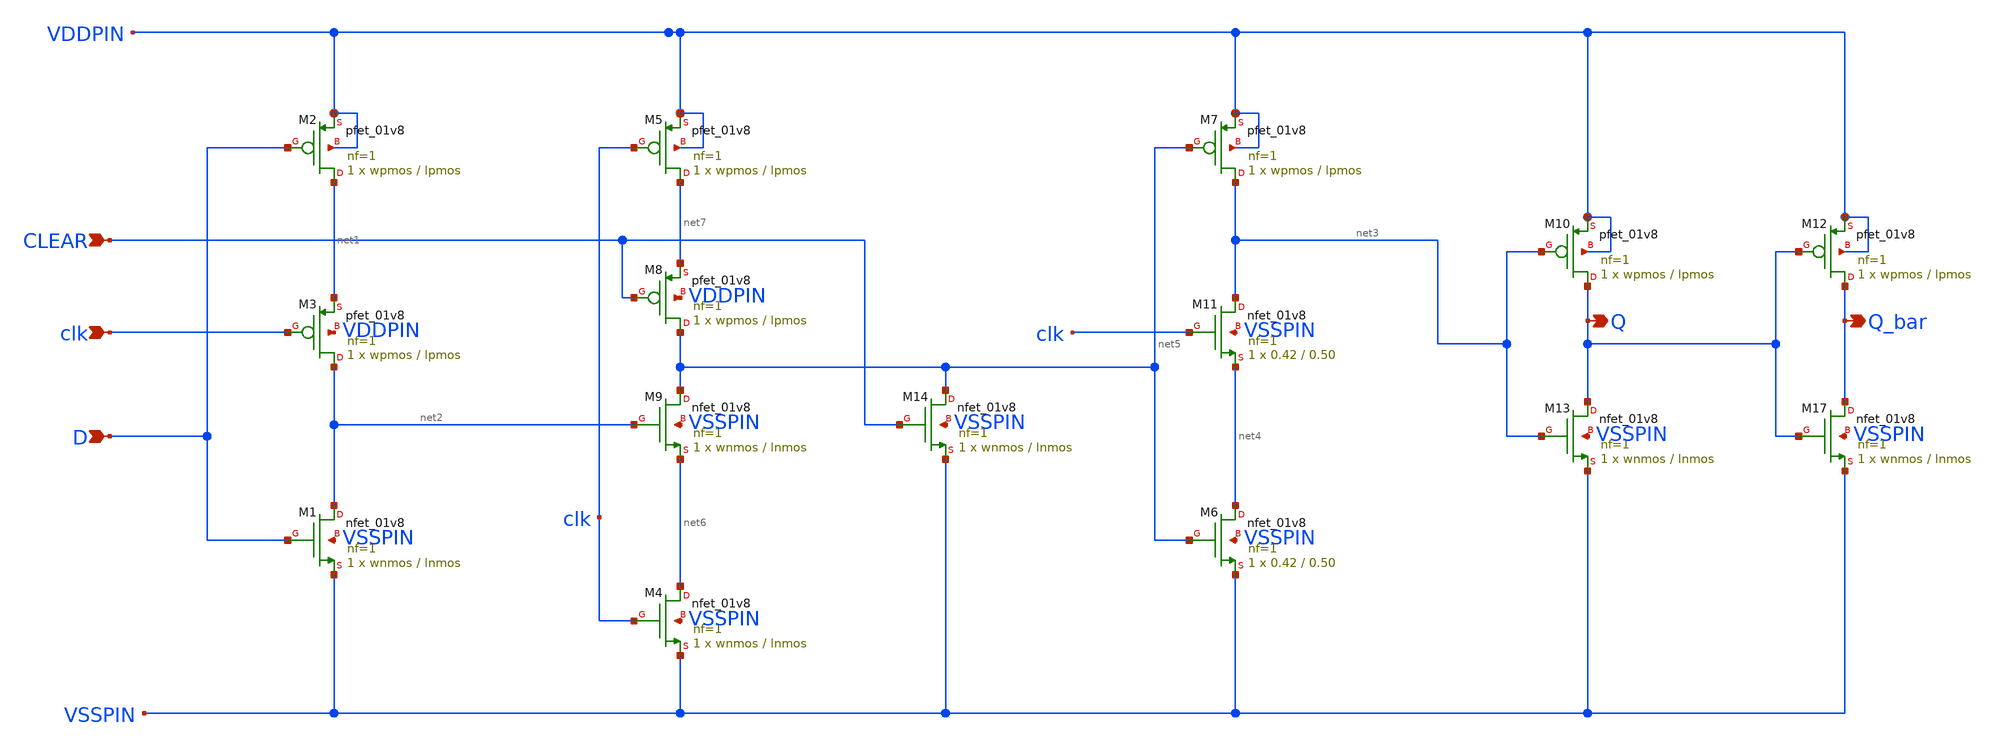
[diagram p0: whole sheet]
** sch_path: TSPC_Dff_with_asynch_clear.sch
**.subckt TSPC_Dff_with_asynch_clear D clk Q Q_bar CLEAR
*.ipin D
*.ipin clk
*.opin Q
*.opin Q_bar
*.ipin CLEAR
XM1 net2 D VSSPIN VSSPIN sky130_fd_pr__nfet_01v8 L=lnmos W=wnmos nf=1 ad='int((nf+1)/2) * W/nf * 0.29'
+ as='int((nf+2)/2) * W/nf * 0.29' pd='2*int((nf+1)/2) * (W/nf + 0.29)' ps='2*int((nf+2)/2) * (W/nf + 0.29)'
+ nrd='0.29 / W' nrs='0.29 / W' sa=0 sb=0 sd=0 mult=1 m=1
XM2 net1 D VDDPIN VDDPIN sky130_fd_pr__pfet_01v8 L=lpmos W=wpmos nf=1 ad='int((nf+1)/2) * W/nf * 0.29'
+ as='int((nf+2)/2) * W/nf * 0.29' pd='2*int((nf+1)/2) * (W/nf + 0.29)' ps='2*int((nf+2)/2) * (W/nf + 0.29)'
+ nrd='0.29 / W' nrs='0.29 / W' sa=0 sb=0 sd=0 mult=1 m=1
XM3 net2 clk net1 VDDPIN sky130_fd_pr__pfet_01v8 L=lpmos W=wpmos nf=1 ad='int((nf+1)/2) * W/nf * 0.29'
+ as='int((nf+2)/2) * W/nf * 0.29' pd='2*int((nf+1)/2) * (W/nf + 0.29)' ps='2*int((nf+2)/2) * (W/nf + 0.29)'
+ nrd='0.29 / W' nrs='0.29 / W' sa=0 sb=0 sd=0 mult=1 m=1
XM4 net6 clk VSSPIN VSSPIN sky130_fd_pr__nfet_01v8 L=lnmos W=wnmos nf=1 ad='int((nf+1)/2) * W/nf * 0.29'
+ as='int((nf+2)/2) * W/nf * 0.29' pd='2*int((nf+1)/2) * (W/nf + 0.29)' ps='2*int((nf+2)/2) * (W/nf + 0.29)'
+ nrd='0.29 / W' nrs='0.29 / W' sa=0 sb=0 sd=0 mult=1 m=1
XM5 net7 clk VDDPIN VDDPIN sky130_fd_pr__pfet_01v8 L=lpmos W=wpmos nf=1 ad='int((nf+1)/2) * W/nf * 0.29'
+ as='int((nf+2)/2) * W/nf * 0.29' pd='2*int((nf+1)/2) * (W/nf + 0.29)' ps='2*int((nf+2)/2) * (W/nf + 0.29)'
+ nrd='0.29 / W' nrs='0.29 / W' sa=0 sb=0 sd=0 mult=1 m=1
XM6 net4 net5 VSSPIN VSSPIN sky130_fd_pr__nfet_01v8 L=0.50 W=0.42 nf=1 ad='int((nf+1)/2) * W/nf * 0.29'
+ as='int((nf+2)/2) * W/nf * 0.29' pd='2*int((nf+1)/2) * (W/nf + 0.29)' ps='2*int((nf+2)/2) * (W/nf + 0.29)'
+ nrd='0.29 / W' nrs='0.29 / W' sa=0 sb=0 sd=0 mult=1 m=1
XM7 net3 net5 VDDPIN VDDPIN sky130_fd_pr__pfet_01v8 L=lpmos W=wpmos nf=1 ad='int((nf+1)/2) * W/nf * 0.29'
+ as='int((nf+2)/2) * W/nf * 0.29' pd='2*int((nf+1)/2) * (W/nf + 0.29)' ps='2*int((nf+2)/2) * (W/nf + 0.29)'
+ nrd='0.29 / W' nrs='0.29 / W' sa=0 sb=0 sd=0 mult=1 m=1
XM9 net5 net2 net6 VSSPIN sky130_fd_pr__nfet_01v8 L=lnmos W=wnmos nf=1 ad='int((nf+1)/2) * W/nf * 0.29'
+ as='int((nf+2)/2) * W/nf * 0.29' pd='2*int((nf+1)/2) * (W/nf + 0.29)' ps='2*int((nf+2)/2) * (W/nf + 0.29)'
+ nrd='0.29 / W' nrs='0.29 / W' sa=0 sb=0 sd=0 mult=1 m=1
XM11 net3 clk net4 VSSPIN sky130_fd_pr__nfet_01v8 L=0.50 W=0.42 nf=1 ad='int((nf+1)/2) * W/nf * 0.29'
+ as='int((nf+2)/2) * W/nf * 0.29' pd='2*int((nf+1)/2) * (W/nf + 0.29)' ps='2*int((nf+2)/2) * (W/nf + 0.29)'
+ nrd='0.29 / W' nrs='0.29 / W' sa=0 sb=0 sd=0 mult=1 m=1
XM10 Q net3 VDDPIN VDDPIN sky130_fd_pr__pfet_01v8 L=lpmos W=wpmos nf=1 ad='int((nf+1)/2) * W/nf * 0.29'
+ as='int((nf+2)/2) * W/nf * 0.29' pd='2*int((nf+1)/2) * (W/nf + 0.29)' ps='2*int((nf+2)/2) * (W/nf + 0.29)'
+ nrd='0.29 / W' nrs='0.29 / W' sa=0 sb=0 sd=0 mult=1 m=1
XM13 Q net3 VSSPIN VSSPIN sky130_fd_pr__nfet_01v8 L=lnmos W=wnmos nf=1 ad='int((nf+1)/2) * W/nf * 0.29'
+ as='int((nf+2)/2) * W/nf * 0.29' pd='2*int((nf+1)/2) * (W/nf + 0.29)' ps='2*int((nf+2)/2) * (W/nf + 0.29)'
+ nrd='0.29 / W' nrs='0.29 / W' sa=0 sb=0 sd=0 mult=1 m=1
XM12 Q_bar Q VDDPIN VDDPIN sky130_fd_pr__pfet_01v8 L=lpmos W=wpmos nf=1 ad='int((nf+1)/2) * W/nf * 0.29'
+ as='int((nf+2)/2) * W/nf * 0.29' pd='2*int((nf+1)/2) * (W/nf + 0.29)' ps='2*int((nf+2)/2) * (W/nf + 0.29)'
+ nrd='0.29 / W' nrs='0.29 / W' sa=0 sb=0 sd=0 mult=1 m=1
XM17 Q_bar Q VSSPIN VSSPIN sky130_fd_pr__nfet_01v8 L=lnmos W=wnmos nf=1 ad='int((nf+1)/2) * W/nf * 0.29'
+ as='int((nf+2)/2) * W/nf * 0.29' pd='2*int((nf+1)/2) * (W/nf + 0.29)' ps='2*int((nf+2)/2) * (W/nf + 0.29)'
+ nrd='0.29 / W' nrs='0.29 / W' sa=0 sb=0 sd=0 mult=1 m=1
XM8 net5 CLEAR net7 VDDPIN sky130_fd_pr__pfet_01v8 L=lpmos W=wpmos nf=1 ad='int((nf+1)/2) * W/nf * 0.29'
+ as='int((nf+2)/2) * W/nf * 0.29' pd='2*int((nf+1)/2) * (W/nf + 0.29)' ps='2*int((nf+2)/2) * (W/nf + 0.29)'
+ nrd='0.29 / W' nrs='0.29 / W' sa=0 sb=0 sd=0 mult=1 m=1
XM14 net5 CLEAR VSSPIN VSSPIN sky130_fd_pr__nfet_01v8 L=lnmos W=wnmos nf=1 ad='int((nf+1)/2) * W/nf * 0.29'
+ as='int((nf+2)/2) * W/nf * 0.29' pd='2*int((nf+1)/2) * (W/nf + 0.29)' ps='2*int((nf+2)/2) * (W/nf + 0.29)'
+ nrd='0.29 / W' nrs='0.29 / W' sa=0 sb=0 sd=0 mult=1 m=1
**.ends
.end
